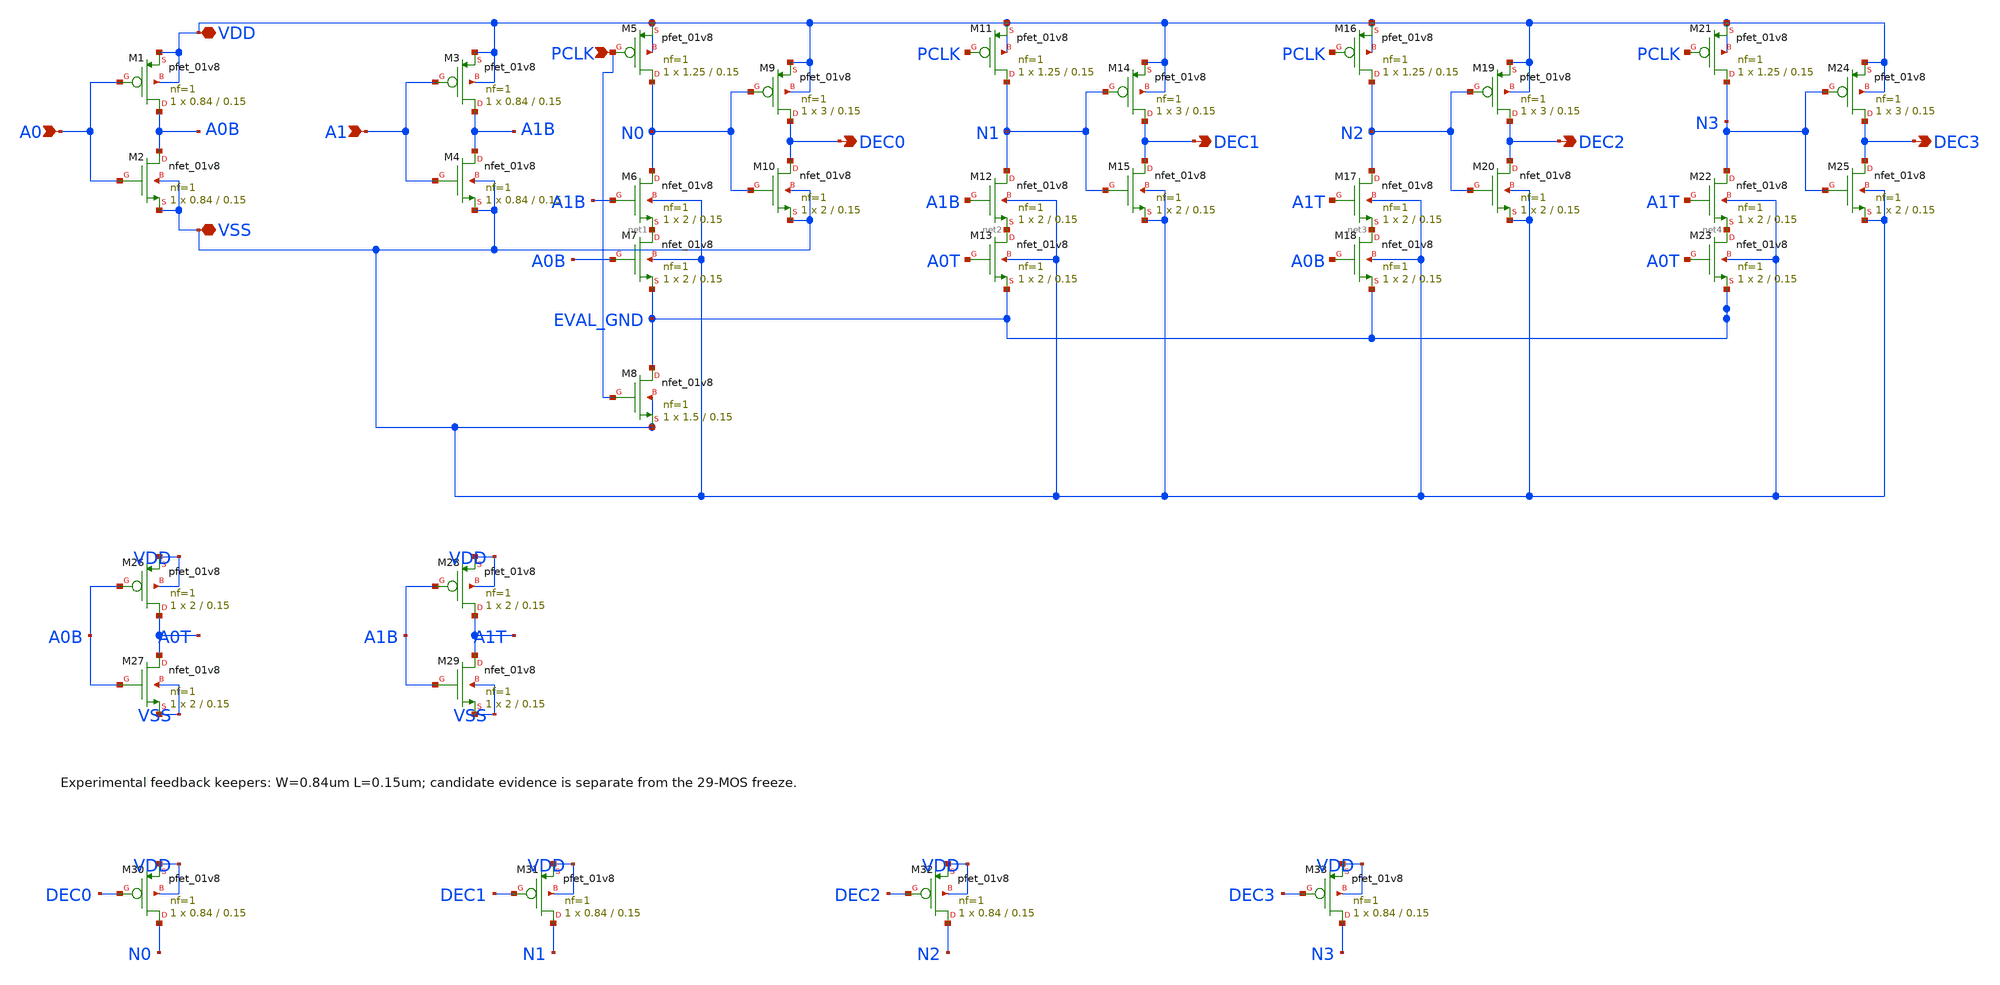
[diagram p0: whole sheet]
** sch_path: release/phase1_keeper/cells/row_decoder/row_decoder.sch
**.subckt row_decoder VDD VSS A0 A1 PCLK DEC0 DEC1 DEC2 DEC3
*.iopin VDD
*.iopin VSS
*.ipin A0
*.ipin A1
*.ipin PCLK
*.opin DEC0
*.opin DEC1
*.opin DEC2
*.opin DEC3
XM1 A0B A0 VDD VDD sky130_fd_pr__pfet_01v8 L=0.15 W=0.84 nf=1 ad='int((nf+1)/2) * W/nf * 0.29' as='int((nf+2)/2) * W/nf * 0.29'
+ pd='2*int((nf+1)/2) * (W/nf + 0.29)' ps='2*int((nf+2)/2) * (W/nf + 0.29)' nrd='0.29 / W' nrs='0.29 / W'
+ sa=0 sb=0 sd=0 mult=1 m=1
XM2 A0B A0 VSS VSS sky130_fd_pr__nfet_01v8 L=0.15 W=0.84 nf=1 ad='int((nf+1)/2) * W/nf * 0.29' as='int((nf+2)/2) * W/nf * 0.29'
+ pd='2*int((nf+1)/2) * (W/nf + 0.29)' ps='2*int((nf+2)/2) * (W/nf + 0.29)' nrd='0.29 / W' nrs='0.29 / W'
+ sa=0 sb=0 sd=0 mult=1 m=1
XM3 A1B A1 VDD VDD sky130_fd_pr__pfet_01v8 L=0.15 W=0.84 nf=1 ad='int((nf+1)/2) * W/nf * 0.29' as='int((nf+2)/2) * W/nf * 0.29'
+ pd='2*int((nf+1)/2) * (W/nf + 0.29)' ps='2*int((nf+2)/2) * (W/nf + 0.29)' nrd='0.29 / W' nrs='0.29 / W'
+ sa=0 sb=0 sd=0 mult=1 m=1
XM4 A1B A1 VSS VSS sky130_fd_pr__nfet_01v8 L=0.15 W=0.84 nf=1 ad='int((nf+1)/2) * W/nf * 0.29' as='int((nf+2)/2) * W/nf * 0.29'
+ pd='2*int((nf+1)/2) * (W/nf + 0.29)' ps='2*int((nf+2)/2) * (W/nf + 0.29)' nrd='0.29 / W' nrs='0.29 / W'
+ sa=0 sb=0 sd=0 mult=1 m=1
XM5 N0 PCLK VDD VDD sky130_fd_pr__pfet_01v8 L=0.15 W=1.25 nf=1 ad='int((nf+1)/2) * W/nf * 0.29' as='int((nf+2)/2) * W/nf * 0.29'
+ pd='2*int((nf+1)/2) * (W/nf + 0.29)' ps='2*int((nf+2)/2) * (W/nf + 0.29)' nrd='0.29 / W' nrs='0.29 / W'
+ sa=0 sb=0 sd=0 mult=1 m=1
XM6 N0 A1B net1 VSS sky130_fd_pr__nfet_01v8 L=0.15 W=2 nf=1 ad='int((nf+1)/2) * W/nf * 0.29' as='int((nf+2)/2) * W/nf * 0.29'
+ pd='2*int((nf+1)/2) * (W/nf + 0.29)' ps='2*int((nf+2)/2) * (W/nf + 0.29)' nrd='0.29 / W' nrs='0.29 / W'
+ sa=0 sb=0 sd=0 mult=1 m=1
XM7 net1 A0B EVAL_GND VSS sky130_fd_pr__nfet_01v8 L=0.15 W=2 nf=1 ad='int((nf+1)/2) * W/nf * 0.29' as='int((nf+2)/2) * W/nf * 0.29'
+ pd='2*int((nf+1)/2) * (W/nf + 0.29)' ps='2*int((nf+2)/2) * (W/nf + 0.29)' nrd='0.29 / W' nrs='0.29 / W'
+ sa=0 sb=0 sd=0 mult=1 m=1
XM8 EVAL_GND PCLK VSS VSS sky130_fd_pr__nfet_01v8 L=0.15 W=1.5 nf=1 ad='int((nf+1)/2) * W/nf * 0.29'
+ as='int((nf+2)/2) * W/nf * 0.29' pd='2*int((nf+1)/2) * (W/nf + 0.29)' ps='2*int((nf+2)/2) * (W/nf + 0.29)'
+ nrd='0.29 / W' nrs='0.29 / W' sa=0 sb=0 sd=0 mult=1 m=1
XM9 DEC0 N0 VDD VDD sky130_fd_pr__pfet_01v8 L=0.15 W=3 nf=1 ad='int((nf+1)/2) * W/nf * 0.29' as='int((nf+2)/2) * W/nf * 0.29'
+ pd='2*int((nf+1)/2) * (W/nf + 0.29)' ps='2*int((nf+2)/2) * (W/nf + 0.29)' nrd='0.29 / W' nrs='0.29 / W'
+ sa=0 sb=0 sd=0 mult=1 m=1
XM10 DEC0 N0 VSS VSS sky130_fd_pr__nfet_01v8 L=0.15 W=2 nf=1 ad='int((nf+1)/2) * W/nf * 0.29' as='int((nf+2)/2) * W/nf * 0.29'
+ pd='2*int((nf+1)/2) * (W/nf + 0.29)' ps='2*int((nf+2)/2) * (W/nf + 0.29)' nrd='0.29 / W' nrs='0.29 / W'
+ sa=0 sb=0 sd=0 mult=1 m=1
XM11 N1 PCLK VDD VDD sky130_fd_pr__pfet_01v8 L=0.15 W=1.25 nf=1 ad='int((nf+1)/2) * W/nf * 0.29' as='int((nf+2)/2) * W/nf * 0.29'
+ pd='2*int((nf+1)/2) * (W/nf + 0.29)' ps='2*int((nf+2)/2) * (W/nf + 0.29)' nrd='0.29 / W' nrs='0.29 / W'
+ sa=0 sb=0 sd=0 mult=1 m=1
XM12 N1 A1B net2 VSS sky130_fd_pr__nfet_01v8 L=0.15 W=2 nf=1 ad='int((nf+1)/2) * W/nf * 0.29' as='int((nf+2)/2) * W/nf * 0.29'
+ pd='2*int((nf+1)/2) * (W/nf + 0.29)' ps='2*int((nf+2)/2) * (W/nf + 0.29)' nrd='0.29 / W' nrs='0.29 / W'
+ sa=0 sb=0 sd=0 mult=1 m=1
XM13 net2 A0T EVAL_GND VSS sky130_fd_pr__nfet_01v8 L=0.15 W=2 nf=1 ad='int((nf+1)/2) * W/nf * 0.29' as='int((nf+2)/2) * W/nf * 0.29'
+ pd='2*int((nf+1)/2) * (W/nf + 0.29)' ps='2*int((nf+2)/2) * (W/nf + 0.29)' nrd='0.29 / W' nrs='0.29 / W'
+ sa=0 sb=0 sd=0 mult=1 m=1
XM14 DEC1 N1 VDD VDD sky130_fd_pr__pfet_01v8 L=0.15 W=3 nf=1 ad='int((nf+1)/2) * W/nf * 0.29' as='int((nf+2)/2) * W/nf * 0.29'
+ pd='2*int((nf+1)/2) * (W/nf + 0.29)' ps='2*int((nf+2)/2) * (W/nf + 0.29)' nrd='0.29 / W' nrs='0.29 / W'
+ sa=0 sb=0 sd=0 mult=1 m=1
XM15 DEC1 N1 VSS VSS sky130_fd_pr__nfet_01v8 L=0.15 W=2 nf=1 ad='int((nf+1)/2) * W/nf * 0.29' as='int((nf+2)/2) * W/nf * 0.29'
+ pd='2*int((nf+1)/2) * (W/nf + 0.29)' ps='2*int((nf+2)/2) * (W/nf + 0.29)' nrd='0.29 / W' nrs='0.29 / W'
+ sa=0 sb=0 sd=0 mult=1 m=1
XM16 N2 PCLK VDD VDD sky130_fd_pr__pfet_01v8 L=0.15 W=1.25 nf=1 ad='int((nf+1)/2) * W/nf * 0.29' as='int((nf+2)/2) * W/nf * 0.29'
+ pd='2*int((nf+1)/2) * (W/nf + 0.29)' ps='2*int((nf+2)/2) * (W/nf + 0.29)' nrd='0.29 / W' nrs='0.29 / W'
+ sa=0 sb=0 sd=0 mult=1 m=1
XM17 N2 A1T net3 VSS sky130_fd_pr__nfet_01v8 L=0.15 W=2 nf=1 ad='int((nf+1)/2) * W/nf * 0.29' as='int((nf+2)/2) * W/nf * 0.29'
+ pd='2*int((nf+1)/2) * (W/nf + 0.29)' ps='2*int((nf+2)/2) * (W/nf + 0.29)' nrd='0.29 / W' nrs='0.29 / W'
+ sa=0 sb=0 sd=0 mult=1 m=1
XM18 net3 A0B EVAL_GND VSS sky130_fd_pr__nfet_01v8 L=0.15 W=2 nf=1 ad='int((nf+1)/2) * W/nf * 0.29' as='int((nf+2)/2) * W/nf * 0.29'
+ pd='2*int((nf+1)/2) * (W/nf + 0.29)' ps='2*int((nf+2)/2) * (W/nf + 0.29)' nrd='0.29 / W' nrs='0.29 / W'
+ sa=0 sb=0 sd=0 mult=1 m=1
XM19 DEC2 N2 VDD VDD sky130_fd_pr__pfet_01v8 L=0.15 W=3 nf=1 ad='int((nf+1)/2) * W/nf * 0.29' as='int((nf+2)/2) * W/nf * 0.29'
+ pd='2*int((nf+1)/2) * (W/nf + 0.29)' ps='2*int((nf+2)/2) * (W/nf + 0.29)' nrd='0.29 / W' nrs='0.29 / W'
+ sa=0 sb=0 sd=0 mult=1 m=1
XM20 DEC2 N2 VSS VSS sky130_fd_pr__nfet_01v8 L=0.15 W=2 nf=1 ad='int((nf+1)/2) * W/nf * 0.29' as='int((nf+2)/2) * W/nf * 0.29'
+ pd='2*int((nf+1)/2) * (W/nf + 0.29)' ps='2*int((nf+2)/2) * (W/nf + 0.29)' nrd='0.29 / W' nrs='0.29 / W'
+ sa=0 sb=0 sd=0 mult=1 m=1
XM21 N3 PCLK VDD VDD sky130_fd_pr__pfet_01v8 L=0.15 W=1.25 nf=1 ad='int((nf+1)/2) * W/nf * 0.29' as='int((nf+2)/2) * W/nf * 0.29'
+ pd='2*int((nf+1)/2) * (W/nf + 0.29)' ps='2*int((nf+2)/2) * (W/nf + 0.29)' nrd='0.29 / W' nrs='0.29 / W'
+ sa=0 sb=0 sd=0 mult=1 m=1
XM22 N3 A1T net4 VSS sky130_fd_pr__nfet_01v8 L=0.15 W=2 nf=1 ad='int((nf+1)/2) * W/nf * 0.29' as='int((nf+2)/2) * W/nf * 0.29'
+ pd='2*int((nf+1)/2) * (W/nf + 0.29)' ps='2*int((nf+2)/2) * (W/nf + 0.29)' nrd='0.29 / W' nrs='0.29 / W'
+ sa=0 sb=0 sd=0 mult=1 m=1
XM23 net4 A0T EVAL_GND VSS sky130_fd_pr__nfet_01v8 L=0.15 W=2 nf=1 ad='int((nf+1)/2) * W/nf * 0.29' as='int((nf+2)/2) * W/nf * 0.29'
+ pd='2*int((nf+1)/2) * (W/nf + 0.29)' ps='2*int((nf+2)/2) * (W/nf + 0.29)' nrd='0.29 / W' nrs='0.29 / W'
+ sa=0 sb=0 sd=0 mult=1 m=1
XM24 DEC3 N3 VDD VDD sky130_fd_pr__pfet_01v8 L=0.15 W=3 nf=1 ad='int((nf+1)/2) * W/nf * 0.29' as='int((nf+2)/2) * W/nf * 0.29'
+ pd='2*int((nf+1)/2) * (W/nf + 0.29)' ps='2*int((nf+2)/2) * (W/nf + 0.29)' nrd='0.29 / W' nrs='0.29 / W'
+ sa=0 sb=0 sd=0 mult=1 m=1
XM25 DEC3 N3 VSS VSS sky130_fd_pr__nfet_01v8 L=0.15 W=2 nf=1 ad='int((nf+1)/2) * W/nf * 0.29' as='int((nf+2)/2) * W/nf * 0.29'
+ pd='2*int((nf+1)/2) * (W/nf + 0.29)' ps='2*int((nf+2)/2) * (W/nf + 0.29)' nrd='0.29 / W' nrs='0.29 / W'
+ sa=0 sb=0 sd=0 mult=1 m=1
XM26 A0T A0B VDD VDD sky130_fd_pr__pfet_01v8 L=0.15 W=2 nf=1 ad='int((nf+1)/2) * W/nf * 0.29' as='int((nf+2)/2) * W/nf * 0.29'
+ pd='2*int((nf+1)/2) * (W/nf + 0.29)' ps='2*int((nf+2)/2) * (W/nf + 0.29)' nrd='0.29 / W' nrs='0.29 / W'
+ sa=0 sb=0 sd=0 mult=1 m=1
XM27 A0T A0B VSS VSS sky130_fd_pr__nfet_01v8 L=0.15 W=2 nf=1 ad='int((nf+1)/2) * W/nf * 0.29' as='int((nf+2)/2) * W/nf * 0.29'
+ pd='2*int((nf+1)/2) * (W/nf + 0.29)' ps='2*int((nf+2)/2) * (W/nf + 0.29)' nrd='0.29 / W' nrs='0.29 / W'
+ sa=0 sb=0 sd=0 mult=1 m=1
XM28 A1T A1B VDD VDD sky130_fd_pr__pfet_01v8 L=0.15 W=2 nf=1 ad='int((nf+1)/2) * W/nf * 0.29' as='int((nf+2)/2) * W/nf * 0.29'
+ pd='2*int((nf+1)/2) * (W/nf + 0.29)' ps='2*int((nf+2)/2) * (W/nf + 0.29)' nrd='0.29 / W' nrs='0.29 / W'
+ sa=0 sb=0 sd=0 mult=1 m=1
XM29 A1T A1B VSS VSS sky130_fd_pr__nfet_01v8 L=0.15 W=2 nf=1 ad='int((nf+1)/2) * W/nf * 0.29' as='int((nf+2)/2) * W/nf * 0.29'
+ pd='2*int((nf+1)/2) * (W/nf + 0.29)' ps='2*int((nf+2)/2) * (W/nf + 0.29)' nrd='0.29 / W' nrs='0.29 / W'
+ sa=0 sb=0 sd=0 mult=1 m=1
XM30 N0 DEC0 VDD VDD sky130_fd_pr__pfet_01v8 L=0.15 W=0.84 nf=1 ad='int((nf+1)/2) * W/nf * 0.29' as='int((nf+2)/2) * W/nf * 0.29'
+ pd='2*int((nf+1)/2) * (W/nf + 0.29)' ps='2*int((nf+2)/2) * (W/nf + 0.29)' nrd='0.29 / W' nrs='0.29 / W'
+ sa=0 sb=0 sd=0 mult=1 m=1
XM31 N1 DEC1 VDD VDD sky130_fd_pr__pfet_01v8 L=0.15 W=0.84 nf=1 ad='int((nf+1)/2) * W/nf * 0.29' as='int((nf+2)/2) * W/nf * 0.29'
+ pd='2*int((nf+1)/2) * (W/nf + 0.29)' ps='2*int((nf+2)/2) * (W/nf + 0.29)' nrd='0.29 / W' nrs='0.29 / W'
+ sa=0 sb=0 sd=0 mult=1 m=1
XM32 N2 DEC2 VDD VDD sky130_fd_pr__pfet_01v8 L=0.15 W=0.84 nf=1 ad='int((nf+1)/2) * W/nf * 0.29' as='int((nf+2)/2) * W/nf * 0.29'
+ pd='2*int((nf+1)/2) * (W/nf + 0.29)' ps='2*int((nf+2)/2) * (W/nf + 0.29)' nrd='0.29 / W' nrs='0.29 / W'
+ sa=0 sb=0 sd=0 mult=1 m=1
XM33 N3 DEC3 VDD VDD sky130_fd_pr__pfet_01v8 L=0.15 W=0.84 nf=1 ad='int((nf+1)/2) * W/nf * 0.29' as='int((nf+2)/2) * W/nf * 0.29'
+ pd='2*int((nf+1)/2) * (W/nf + 0.29)' ps='2*int((nf+2)/2) * (W/nf + 0.29)' nrd='0.29 / W' nrs='0.29 / W'
+ sa=0 sb=0 sd=0 mult=1 m=1
**.ends
.end
